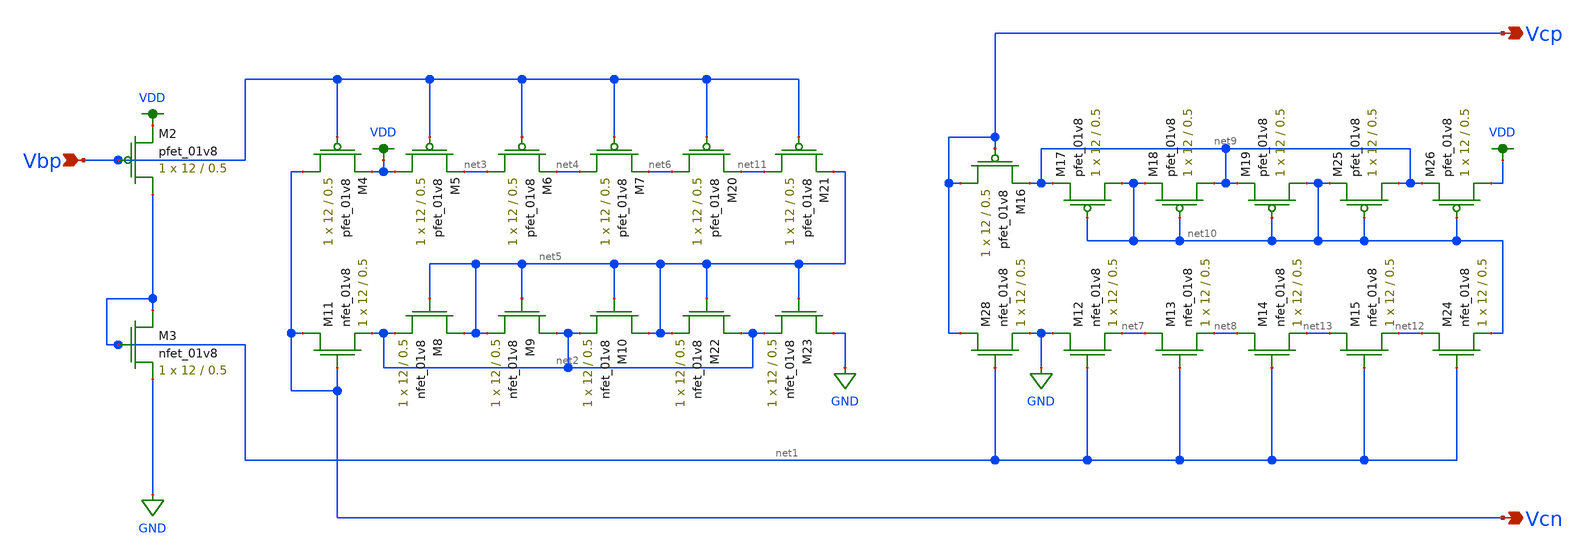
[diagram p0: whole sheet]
** sch_path: modules/bias_current_generator.sch
**.subckt bias_current_generator Vcn Vcp Vbp
*.opin Vcn
*.opin Vcp
*.ipin Vbp
XM4 Vcn Vbp VDD VDD sky130_fd_pr__pfet_01v8 L=0.5 W=12 nf=1 ad='int((nf+1)/2) * W/nf * 0.29' as='int((nf+2)/2) * W/nf * 0.29'
+ pd='2*int((nf+1)/2) * (W/nf + 0.29)' ps='2*int((nf+2)/2) * (W/nf + 0.29)' nrd='0.29 / W' nrs='0.29 / W'
+ sa=0 sb=0 sd=0 mult=1 m=1
XM11 Vcn Vcn net2 GND sky130_fd_pr__nfet_01v8 L=0.5 W=12 nf=1 ad='int((nf+1)/2) * W/nf * 0.29' as='int((nf+2)/2) * W/nf * 0.29'
+ pd='2*int((nf+1)/2) * (W/nf + 0.29)' ps='2*int((nf+2)/2) * (W/nf + 0.29)' nrd='0.29 / W' nrs='0.29 / W'
+ sa=0 sb=0 sd=0 mult=1 m=1
XM8 net5 net5 net2 GND sky130_fd_pr__nfet_01v8 L=0.5 W=12 nf=1 ad='int((nf+1)/2) * W/nf * 0.29' as='int((nf+2)/2) * W/nf * 0.29'
+ pd='2*int((nf+1)/2) * (W/nf + 0.29)' ps='2*int((nf+2)/2) * (W/nf + 0.29)' nrd='0.29 / W' nrs='0.29 / W'
+ sa=0 sb=0 sd=0 mult=1 m=1
XM9 net2 net5 net5 GND sky130_fd_pr__nfet_01v8 L=0.5 W=12 nf=1 ad='int((nf+1)/2) * W/nf * 0.29' as='int((nf+2)/2) * W/nf * 0.29'
+ pd='2*int((nf+1)/2) * (W/nf + 0.29)' ps='2*int((nf+2)/2) * (W/nf + 0.29)' nrd='0.29 / W' nrs='0.29 / W'
+ sa=0 sb=0 sd=0 mult=1 m=1
XM10 net5 net5 net2 GND sky130_fd_pr__nfet_01v8 L=0.5 W=12 nf=1 ad='int((nf+1)/2) * W/nf * 0.29' as='int((nf+2)/2) * W/nf * 0.29'
+ pd='2*int((nf+1)/2) * (W/nf + 0.29)' ps='2*int((nf+2)/2) * (W/nf + 0.29)' nrd='0.29 / W' nrs='0.29 / W'
+ sa=0 sb=0 sd=0 mult=1 m=1
XM22 net2 net5 net5 GND sky130_fd_pr__nfet_01v8 L=0.5 W=12 nf=1 ad='int((nf+1)/2) * W/nf * 0.29' as='int((nf+2)/2) * W/nf * 0.29'
+ pd='2*int((nf+1)/2) * (W/nf + 0.29)' ps='2*int((nf+2)/2) * (W/nf + 0.29)' nrd='0.29 / W' nrs='0.29 / W'
+ sa=0 sb=0 sd=0 mult=1 m=1
XM23 GND net5 net2 GND sky130_fd_pr__nfet_01v8 L=0.5 W=12 nf=1 ad='int((nf+1)/2) * W/nf * 0.29' as='int((nf+2)/2) * W/nf * 0.29'
+ pd='2*int((nf+1)/2) * (W/nf + 0.29)' ps='2*int((nf+2)/2) * (W/nf + 0.29)' nrd='0.29 / W' nrs='0.29 / W'
+ sa=0 sb=0 sd=0 mult=1 m=1
XM28 Vcp net1 GND GND sky130_fd_pr__nfet_01v8 L=0.5 W=12 nf=1 ad='int((nf+1)/2) * W/nf * 0.29' as='int((nf+2)/2) * W/nf * 0.29'
+ pd='2*int((nf+1)/2) * (W/nf + 0.29)' ps='2*int((nf+2)/2) * (W/nf + 0.29)' nrd='0.29 / W' nrs='0.29 / W'
+ sa=0 sb=0 sd=0 mult=1 m=1
XM12 GND net1 net7 GND sky130_fd_pr__nfet_01v8 L=0.5 W=12 nf=1 ad='int((nf+1)/2) * W/nf * 0.29' as='int((nf+2)/2) * W/nf * 0.29'
+ pd='2*int((nf+1)/2) * (W/nf + 0.29)' ps='2*int((nf+2)/2) * (W/nf + 0.29)' nrd='0.29 / W' nrs='0.29 / W'
+ sa=0 sb=0 sd=0 mult=1 m=1
XM13 net7 net1 net8 GND sky130_fd_pr__nfet_01v8 L=0.5 W=12 nf=1 ad='int((nf+1)/2) * W/nf * 0.29' as='int((nf+2)/2) * W/nf * 0.29'
+ pd='2*int((nf+1)/2) * (W/nf + 0.29)' ps='2*int((nf+2)/2) * (W/nf + 0.29)' nrd='0.29 / W' nrs='0.29 / W'
+ sa=0 sb=0 sd=0 mult=1 m=1
XM14 net8 net1 net13 GND sky130_fd_pr__nfet_01v8 L=0.5 W=12 nf=1 ad='int((nf+1)/2) * W/nf * 0.29' as='int((nf+2)/2) * W/nf * 0.29'
+ pd='2*int((nf+1)/2) * (W/nf + 0.29)' ps='2*int((nf+2)/2) * (W/nf + 0.29)' nrd='0.29 / W' nrs='0.29 / W'
+ sa=0 sb=0 sd=0 mult=1 m=1
XM15 net13 net1 net12 GND sky130_fd_pr__nfet_01v8 L=0.5 W=12 nf=1 ad='int((nf+1)/2) * W/nf * 0.29' as='int((nf+2)/2) * W/nf * 0.29'
+ pd='2*int((nf+1)/2) * (W/nf + 0.29)' ps='2*int((nf+2)/2) * (W/nf + 0.29)' nrd='0.29 / W' nrs='0.29 / W'
+ sa=0 sb=0 sd=0 mult=1 m=1
XM24 net12 net1 net10 GND sky130_fd_pr__nfet_01v8 L=0.5 W=12 nf=1 ad='int((nf+1)/2) * W/nf * 0.29' as='int((nf+2)/2) * W/nf * 0.29'
+ pd='2*int((nf+1)/2) * (W/nf + 0.29)' ps='2*int((nf+2)/2) * (W/nf + 0.29)' nrd='0.29 / W' nrs='0.29 / W'
+ sa=0 sb=0 sd=0 mult=1 m=1
XM5 VDD Vbp net3 VDD sky130_fd_pr__pfet_01v8 L=0.5 W=12 nf=1 ad='int((nf+1)/2) * W/nf * 0.29' as='int((nf+2)/2) * W/nf * 0.29'
+ pd='2*int((nf+1)/2) * (W/nf + 0.29)' ps='2*int((nf+2)/2) * (W/nf + 0.29)' nrd='0.29 / W' nrs='0.29 / W'
+ sa=0 sb=0 sd=0 mult=1 m=1
XM6 net3 Vbp net4 VDD sky130_fd_pr__pfet_01v8 L=0.5 W=12 nf=1 ad='int((nf+1)/2) * W/nf * 0.29' as='int((nf+2)/2) * W/nf * 0.29'
+ pd='2*int((nf+1)/2) * (W/nf + 0.29)' ps='2*int((nf+2)/2) * (W/nf + 0.29)' nrd='0.29 / W' nrs='0.29 / W'
+ sa=0 sb=0 sd=0 mult=1 m=1
XM7 net4 Vbp net6 VDD sky130_fd_pr__pfet_01v8 L=0.5 W=12 nf=1 ad='int((nf+1)/2) * W/nf * 0.29' as='int((nf+2)/2) * W/nf * 0.29'
+ pd='2*int((nf+1)/2) * (W/nf + 0.29)' ps='2*int((nf+2)/2) * (W/nf + 0.29)' nrd='0.29 / W' nrs='0.29 / W'
+ sa=0 sb=0 sd=0 mult=1 m=1
XM20 net6 Vbp net11 VDD sky130_fd_pr__pfet_01v8 L=0.5 W=12 nf=1 ad='int((nf+1)/2) * W/nf * 0.29' as='int((nf+2)/2) * W/nf * 0.29'
+ pd='2*int((nf+1)/2) * (W/nf + 0.29)' ps='2*int((nf+2)/2) * (W/nf + 0.29)' nrd='0.29 / W' nrs='0.29 / W'
+ sa=0 sb=0 sd=0 mult=1 m=1
XM21 net11 Vbp net5 VDD sky130_fd_pr__pfet_01v8 L=0.5 W=12 nf=1 ad='int((nf+1)/2) * W/nf * 0.29' as='int((nf+2)/2) * W/nf * 0.29'
+ pd='2*int((nf+1)/2) * (W/nf + 0.29)' ps='2*int((nf+2)/2) * (W/nf + 0.29)' nrd='0.29 / W' nrs='0.29 / W'
+ sa=0 sb=0 sd=0 mult=1 m=1
XM16 Vcp Vcp net9 VDD sky130_fd_pr__pfet_01v8 L=0.5 W=12 nf=1 ad='int((nf+1)/2) * W/nf * 0.29' as='int((nf+2)/2) * W/nf * 0.29'
+ pd='2*int((nf+1)/2) * (W/nf + 0.29)' ps='2*int((nf+2)/2) * (W/nf + 0.29)' nrd='0.29 / W' nrs='0.29 / W'
+ sa=0 sb=0 sd=0 mult=1 m=1
XM17 net10 net10 net9 VDD sky130_fd_pr__pfet_01v8 L=0.5 W=12 nf=1 ad='int((nf+1)/2) * W/nf * 0.29' as='int((nf+2)/2) * W/nf * 0.29'
+ pd='2*int((nf+1)/2) * (W/nf + 0.29)' ps='2*int((nf+2)/2) * (W/nf + 0.29)' nrd='0.29 / W' nrs='0.29 / W'
+ sa=0 sb=0 sd=0 mult=1 m=1
XM18 net9 net10 net10 VDD sky130_fd_pr__pfet_01v8 L=0.5 W=12 nf=1 ad='int((nf+1)/2) * W/nf * 0.29' as='int((nf+2)/2) * W/nf * 0.29'
+ pd='2*int((nf+1)/2) * (W/nf + 0.29)' ps='2*int((nf+2)/2) * (W/nf + 0.29)' nrd='0.29 / W' nrs='0.29 / W'
+ sa=0 sb=0 sd=0 mult=1 m=1
XM19 net10 net10 net9 VDD sky130_fd_pr__pfet_01v8 L=0.5 W=12 nf=1 ad='int((nf+1)/2) * W/nf * 0.29' as='int((nf+2)/2) * W/nf * 0.29'
+ pd='2*int((nf+1)/2) * (W/nf + 0.29)' ps='2*int((nf+2)/2) * (W/nf + 0.29)' nrd='0.29 / W' nrs='0.29 / W'
+ sa=0 sb=0 sd=0 mult=1 m=1
XM25 net9 net10 net10 VDD sky130_fd_pr__pfet_01v8 L=0.5 W=12 nf=1 ad='int((nf+1)/2) * W/nf * 0.29' as='int((nf+2)/2) * W/nf * 0.29'
+ pd='2*int((nf+1)/2) * (W/nf + 0.29)' ps='2*int((nf+2)/2) * (W/nf + 0.29)' nrd='0.29 / W' nrs='0.29 / W'
+ sa=0 sb=0 sd=0 mult=1 m=1
XM26 VDD net10 net9 VDD sky130_fd_pr__pfet_01v8 L=0.5 W=12 nf=1 ad='int((nf+1)/2) * W/nf * 0.29' as='int((nf+2)/2) * W/nf * 0.29'
+ pd='2*int((nf+1)/2) * (W/nf + 0.29)' ps='2*int((nf+2)/2) * (W/nf + 0.29)' nrd='0.29 / W' nrs='0.29 / W'
+ sa=0 sb=0 sd=0 mult=1 m=1
XM2 net1 Vbp VDD VDD sky130_fd_pr__pfet_01v8 L=0.5 W=12 nf=1 ad='int((nf+1)/2) * W/nf * 0.29' as='int((nf+2)/2) * W/nf * 0.29'
+ pd='2*int((nf+1)/2) * (W/nf + 0.29)' ps='2*int((nf+2)/2) * (W/nf + 0.29)' nrd='0.29 / W' nrs='0.29 / W'
+ sa=0 sb=0 sd=0 mult=1 m=1
XM3 net1 net1 GND GND sky130_fd_pr__nfet_01v8 L=0.5 W=12 nf=1 ad='int((nf+1)/2) * W/nf * 0.29' as='int((nf+2)/2) * W/nf * 0.29'
+ pd='2*int((nf+1)/2) * (W/nf + 0.29)' ps='2*int((nf+2)/2) * (W/nf + 0.29)' nrd='0.29 / W' nrs='0.29 / W'
+ sa=0 sb=0 sd=0 mult=1 m=1
**.ends
.GLOBAL GND
.GLOBAL VDD
.end
